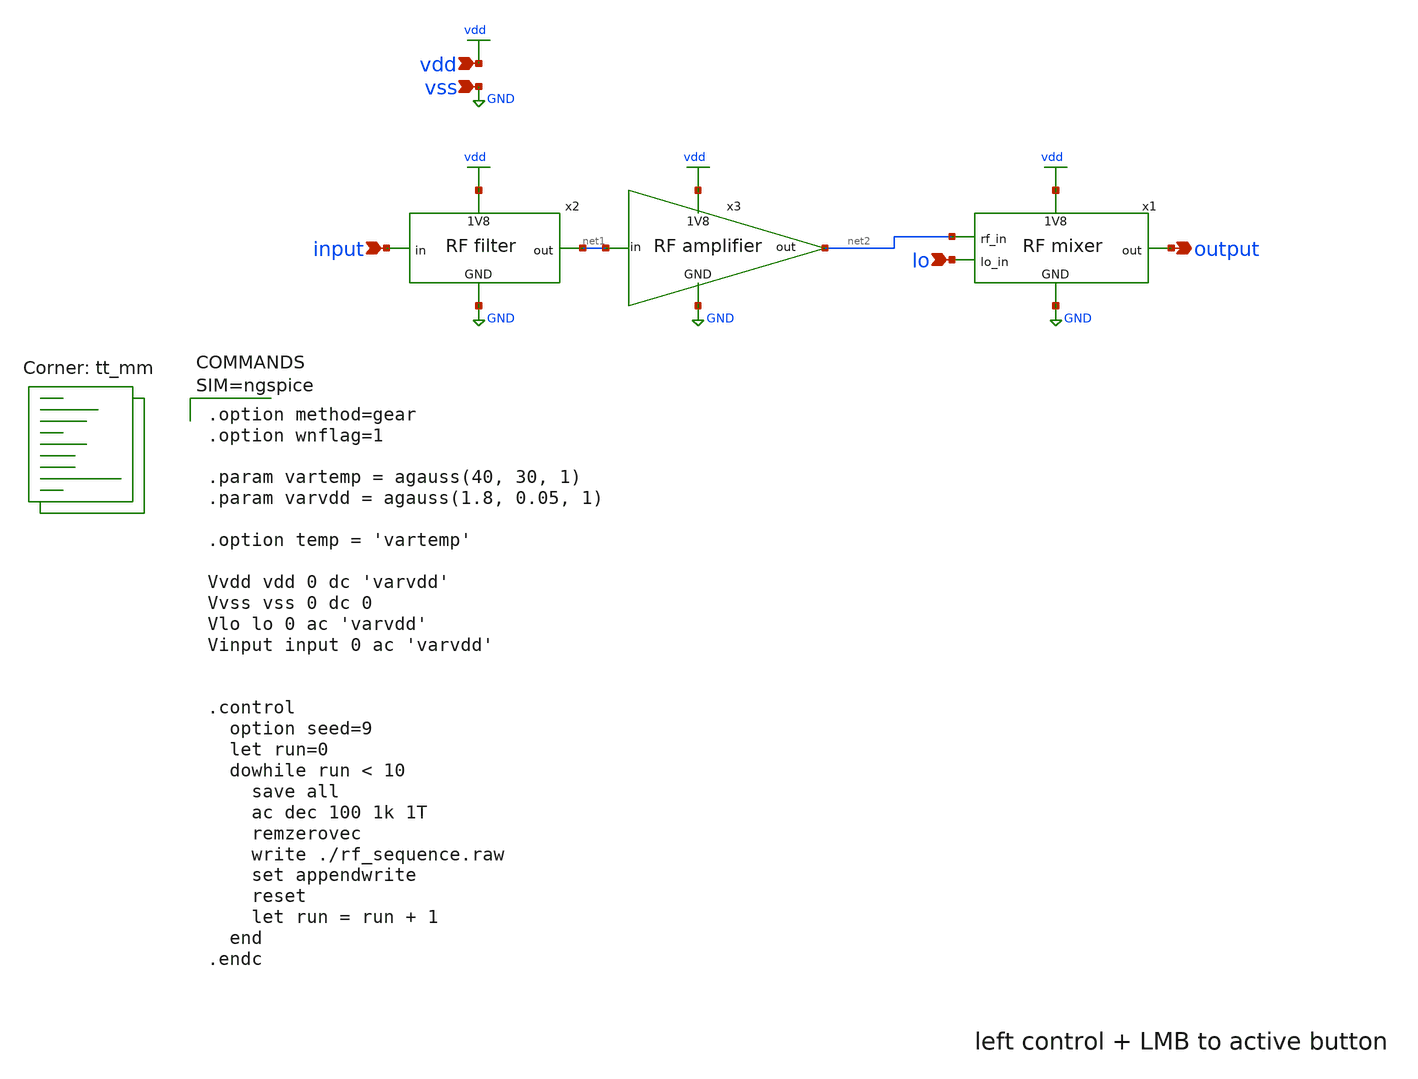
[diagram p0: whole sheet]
** sch_path: tests/rf_sequence.sch
**.subckt rf_sequence input output lo vdd vss
*.ipin input
*.opin output
*.ipin lo
*.ipin vdd
*.ipin vss
x1 net2 lo vdd output GND rf_mixer
x2 vdd input net1 GND rf_filter
x3 vdd net1 net2 GND rf_amplifier
**** begin user architecture code
.lib $::SKYWATER_MODELS/sky130.lib.spice tt_mm


.option method=gear
.option wnflag=1

.param vartemp = agauss(40, 30, 1)
.param varvdd = agauss(1.8, 0.05, 1)

.option temp = 'vartemp'

Vvdd vdd 0 dc 'varvdd'
Vvss vss 0 dc 0
Vlo lo 0 ac 'varvdd'
Vinput input 0 ac 'varvdd'


.control
  option seed=9
  let run=0
  dowhile run < 10
    save all
    ac dec 100 1k 1T
    remzerovec
    write ./rf_sequence.raw
    set appendwrite
    reset
    let run = run + 1
  end
.endc


**** end user architecture code
**.ends

* expanding   symbol:  ./rf_mixer.sym # of pins=5
** sym_path: schematic/rf_mixer.sym
** sch_path: schematic/rf_mixer.sch
.subckt rf_mixer rf_in lo_in 1V8 out GND
*.ipin rf_in
*.opin out
*.ipin GND
*.ipin 1V8
*.ipin lo_in
* noconn 1V8
* noconn GND
* noconn lo_in
R1 out rf_in 0 m=1
.ends


* expanding   symbol:  ./rf_filter.sym # of pins=4
** sym_path: schematic/rf_filter.sym
** sch_path: schematic/rf_filter.sch
.subckt rf_filter 1V8 in out GND
*.ipin in
*.opin out
*.ipin GND
*.ipin 1V8
* noconn 1V8
XR1 GND net1 GND sky130_fd_pr__res_iso_pw W=2.65 L=2.65 m=1
XC1 in net1 sky130_fd_pr__cap_mim_m3_1 W=1 L=1 MF=1 m=1
XR2 net1 out GND sky130_fd_pr__res_iso_pw W=2.65 L=2.65 m=1
XC2 out GND sky130_fd_pr__cap_mim_m3_1 W=1 L=1 MF=1 m=1
.ends


* expanding   symbol:  ./rf_amplifier.sym # of pins=4
** sym_path: schematic/rf_amplifier.sym
** sch_path: schematic/rf_amplifier.sch
.subckt rf_amplifier 1V8 in out GND
*.ipin in
*.opin out
*.ipin GND
*.ipin 1V8
* noconn 1V8
* noconn GND
R1 out in 0 m=1
.ends

.GLOBAL GND
.GLOBAL vdd
.end
